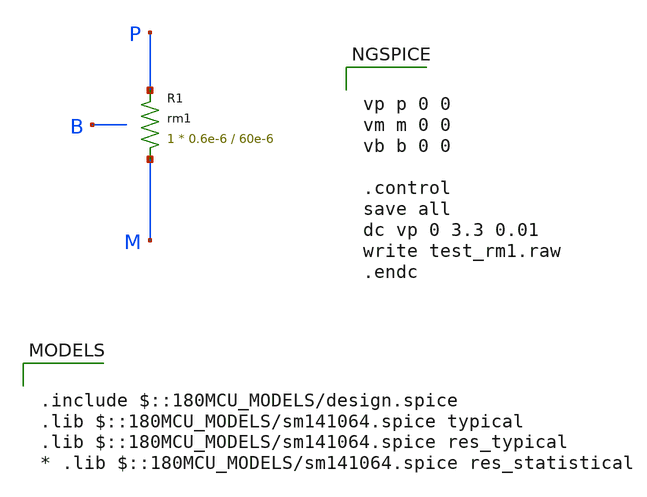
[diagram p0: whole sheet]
** sch_path: cells/xschem/tests/test_rm1.sch
* Copyright 2022 GlobalFoundries PDK Authors
* Licensed under the Apache License, Version 2.0 (the "License");
* you may not use this file except in compliance with the License.
* You may obtain a copy of the License at
* https://www.apache.org/licenses/LICENSE-2.0
* Unless required by applicable law or agreed to in writing, software
* distributed under the License is distributed on an "AS IS" BASIS,
* WITHOUT WARRANTIES OR CONDITIONS OF ANY KIND, either express or implied.
* See the License for the specific language governing permissions and
* limitations under the License.
**.subckt test_rm1
XR1 M P rm1 r_width=0.6e-6 r_length=60e-6 m=1
**** begin user architecture code

.include $::180MCU_MODELS/design.spice
.lib $::180MCU_MODELS/sm141064.spice typical
.lib $::180MCU_MODELS/sm141064.spice res_typical
* .lib $::180MCU_MODELS/sm141064.spice res_statistical



vp p 0 0
vm m 0 0
vb b 0 0

.control
save all
dc vp 0 3.3 0.01
write test_rm1.raw
.endc


**** end user architecture code
**.ends
.end
